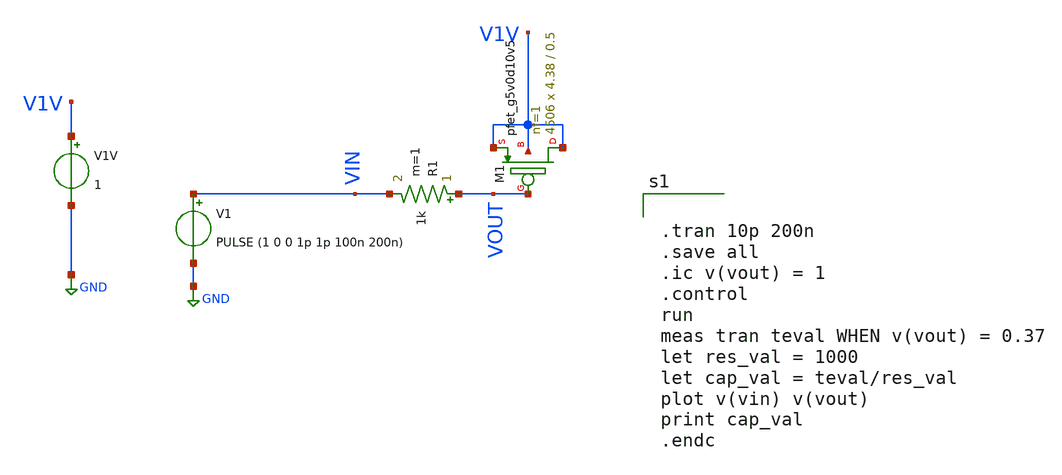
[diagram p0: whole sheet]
** sch_path: xschem/TB_hvPMOS_cgate-ext_SKY130.sch
.lib $::SKYWATER_MODELS/sky130.lib.spice tt
.include $::SKYWATER_STDCELLS/sky130_fd_sc_hd.spice

**.subckt TB_hvPMOS_cgate-ext_SKY130
R1 VOUT VIN 1k m=1
V1 VIN GND PULSE (1 0 0 1p 1p 100n 200n)
V1V V1V GND 1
XM1 V1V VOUT V1V V1V sky130_fd_pr__pfet_g5v0d10v5 L=0.5 W=4.38 nf=1 ad='int((nf+1)/2) * W/nf * 0.29'
+ as='int((nf+2)/2) * W/nf * 0.29' pd='2*int((nf+1)/2) * (W/nf + 0.29)' ps='2*int((nf+2)/2) * (W/nf + 0.29)'
+ nrd='0.29 / W' nrs='0.29 / W' sa=0 sb=0 sd=0 mult=4506 m=4506
**** begin user architecture code


.tran 10p 200n
.save all
.ic v(vout) = 1
.control
run
meas tran teval WHEN v(vout) = 0.37
let res_val = 1000
let cap_val = teval/res_val
plot v(vin) v(vout)
print cap_val
.endc




.param temp=27

.param mult_M2 = 1200
.param w_M2 =10u
*.param l_M2 =0.25u
.param l_M2 =0.25u
.param ng_M2 =1





**** end user architecture code
**.ends
.GLOBAL GND
.end
